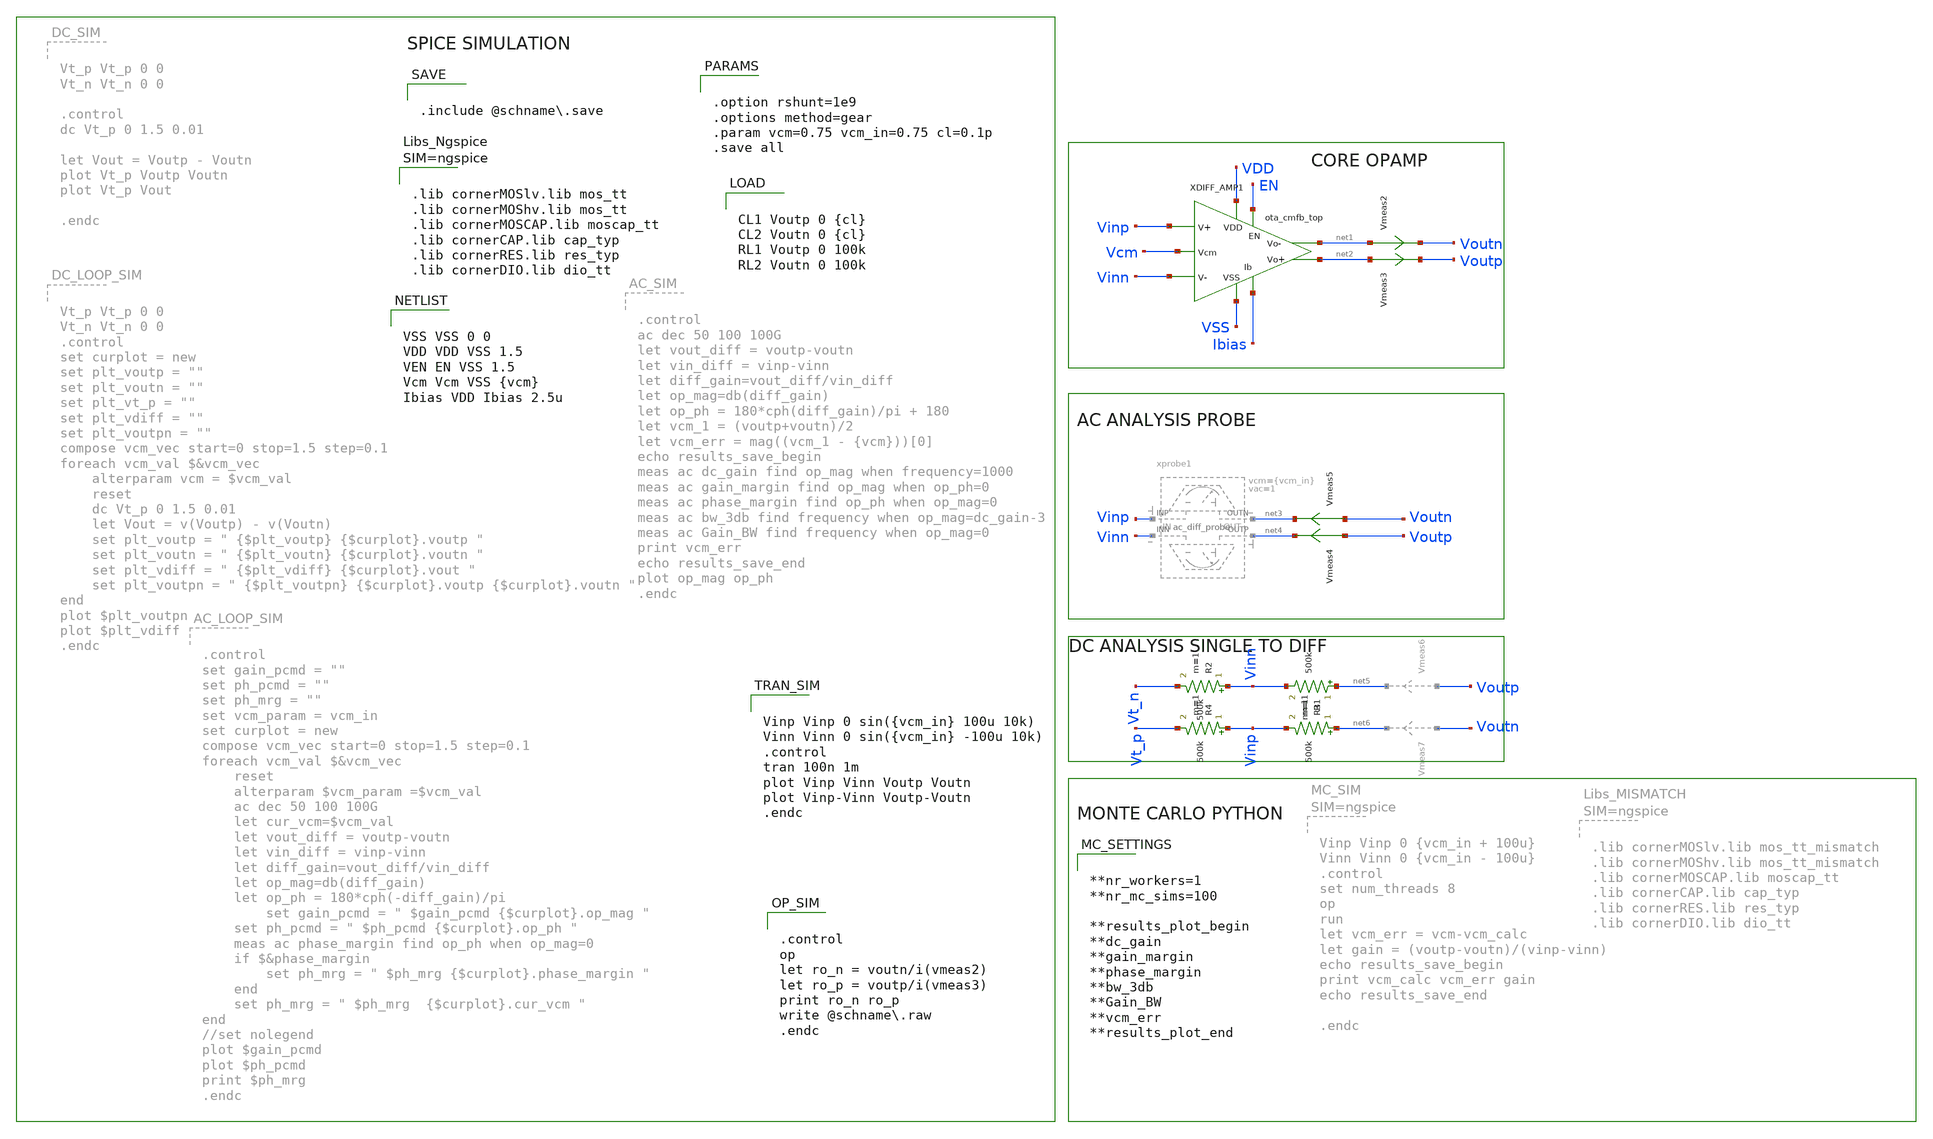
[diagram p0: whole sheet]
** sch_path: schema/ota_cmfb_top_tb.sch
**.subckt ota_cmfb_top_tb
Vmeas2 net1 Voutn 0
.save i(vmeas2)
Vmeas3 net2 Voutp 0
.save i(vmeas3)
Vmeas4 Voutp net4 0
.save i(vmeas4)
Vmeas5 Voutn net3 0
.save i(vmeas5)
R1 net5 Vinn 500k m=1
R2 Vinn Vt_n 500k m=1
R3 net6 Vinp 500k m=1
R4 Vinp Vt_p 500k m=1
XDIFF_AMP1 Vcm VDD EN Vinp net1 net2 Vinn VSS Ibias ota_cmfb_top
**** begin user architecture code


VSS VSS 0 0
VDD VDD VSS 1.5
VEN EN VSS 1.5
Vcm Vcm VSS {vcm}
Ibias VDD Ibias 2.5u



.control
op
let ro_n = voutn/i(vmeas2)
let ro_p = voutp/i(vmeas3)
print ro_n ro_p
write @schname.raw
.endc




.lib cornerMOSlv.lib mos_tt
.lib cornerMOShv.lib mos_tt
.lib cornerMOSCAP.lib moscap_tt
.lib cornerCAP.lib cap_typ
.lib cornerRES.lib res_typ
.lib cornerDIO.lib dio_tt





.option rshunt=1e9
.options method=gear
.param vcm=0.75 vcm_in=0.75 cl=0.1p
.save all




CL1 Voutp 0 {cl}
CL2 Voutn 0 {cl}
RL1 Voutp 0 100k
RL2 Voutn 0 100k



.include @schname.save



Vinp Vinp 0 sin({vcm_in} 100u 10k)
Vinn Vinn 0 sin({vcm_in} -100u 10k)
.control
tran 100n 1m
plot Vinp Vinn Voutp Voutn
plot Vinp-Vinn Voutp-Voutn
.endc




**nr_workers=1
**nr_mc_sims=100

**results_plot_begin
**dc_gain
**gain_margin
**phase_margin
**bw_3db
**Gain_BW
**vcm_err
**results_plot_end


**** end user architecture code
**.ends
.end
